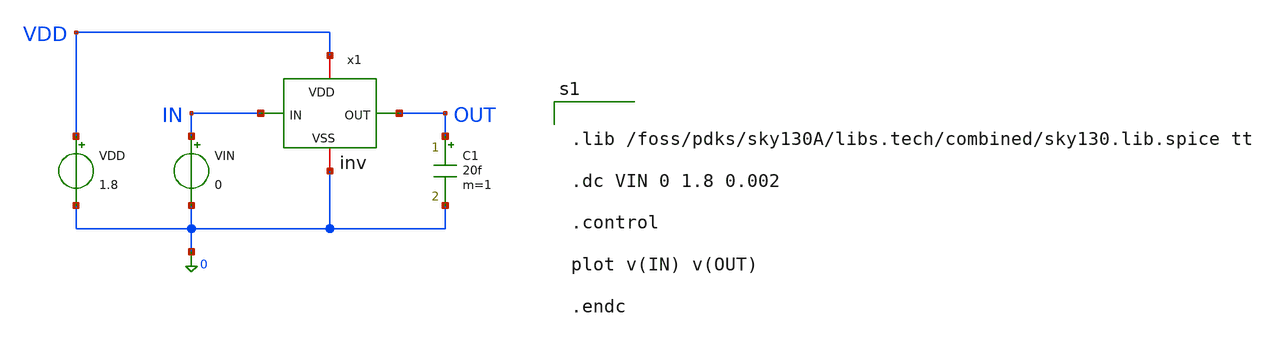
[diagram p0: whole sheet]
** sch_path: schem/inv/inv_tb.sch
**.subckt inv_tb
x1 VDD IN OUT 0 inv
VIN IN 0 0
VDD VDD 0 1.8
C1 OUT 0 20f m=1
**** begin user architecture code


.lib /foss/pdks/sky130A/libs.tech/combined/sky130.lib.spice tt

.dc VIN 0 1.8 0.002

.control

plot v(IN) v(OUT)

.endc


**** end user architecture code
**.ends

* expanding   symbol:  inv.sym # of pins=4
** sym_path: schem/inv/inv.sym
** sch_path: schem/inv/inv.sch
.subckt inv VDD IN OUT VSS
*.ipin IN
*.iopin VDD
*.iopin VSS
*.opin OUT
XM1 OUT IN VSS VSS sky130_fd_pr__nfet_01v8 L=0.5 W=1 nf=1 ad='int((1 + 1)/2) * 1 / 1 * 0.29' as='int((1 + 2)/2) * 1 / 1 * 0.29'
+ pd='2*int((1 + 1)/2) * (1 / 1 + 0.29)' ps='2*int((1 + 2)/2) * (1 / 1 + 0.29)' nrd='0.29 / 1 ' nrs='0.29 / 1 '
+ sa=0 sb=0 sd=0 mult=1 m=1
XM2 OUT IN VDD VDD sky130_fd_pr__pfet_01v8_lvt L=0.5 W=2 nf=1 ad='int((1 + 1)/2) * 2 / 1 * 0.29' as='int((1 + 2)/2) * 2 / 1 * 0.29'
+ pd='2*int((1 + 1)/2) * (2 / 1 + 0.29)' ps='2*int((1 + 2)/2) * (2 / 1 + 0.29)' nrd='0.29 / 2 ' nrs='0.29 / 2 '
+ sa=0 sb=0 sd=0 mult=1 m=1
.ends

.end
